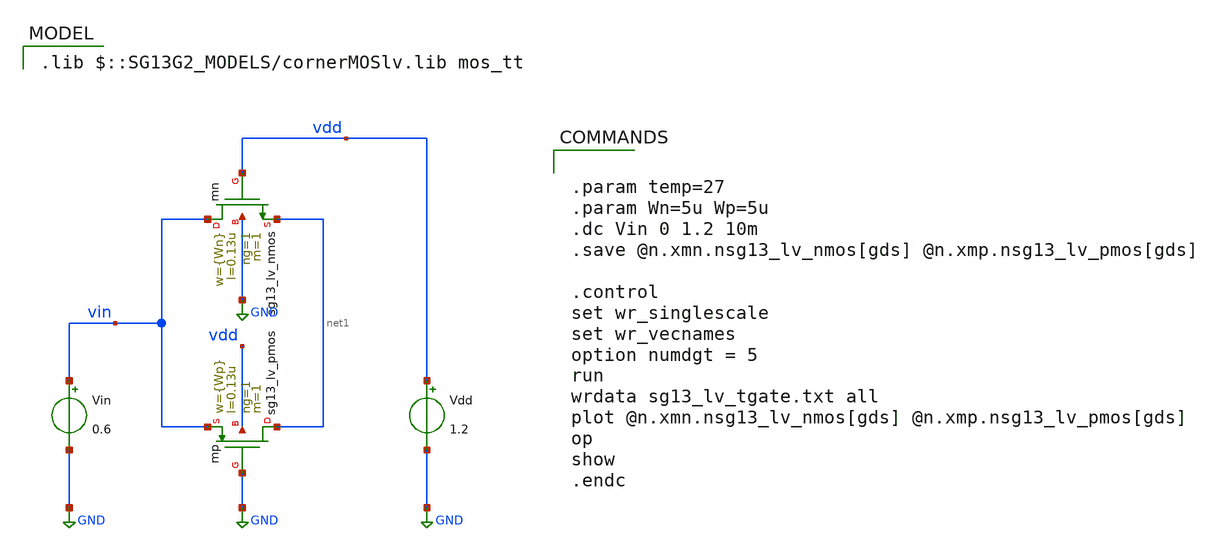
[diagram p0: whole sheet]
** sch_path: 4_Technology/src/tb_sg13_lv_tgate.sch
**.subckt tb_sg13_lv_tgate
Xmn vin vdd net1 GND sg13_lv_nmos w={Wn} l=0.13u ng=1 m=1 mm_ok=1
Vin vin GND 0.6
Vdd vdd GND 1.2
Xmp net1 GND vin vdd sg13_lv_pmos w={Wp} l=0.13u ng=1 m=1 mm_ok=1
**** begin user architecture code
 .lib $::SG13G2_MODELS/cornerMOSlv.lib mos_tt



.param temp=27
.param Wn=5u Wp=5u
.dc Vin 0 1.2 10m
.save @n.xmn.nsg13_lv_nmos[gds] @n.xmp.nsg13_lv_pmos[gds]

.control
set wr_singlescale
set wr_vecnames
option numdgt = 5
run
wrdata sg13_lv_tgate.txt all
plot @n.xmn.nsg13_lv_nmos[gds] @n.xmp.nsg13_lv_pmos[gds]
op
show
.endc


**** end user architecture code
**.ends
.GLOBAL GND
.end
